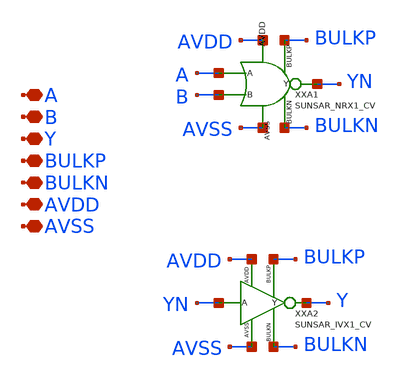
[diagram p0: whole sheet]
** sch_path: design/SUN_SAR9B_SKY130NM/SUNSAR_ORX1_CV.sch
**.subckt SUNSAR_ORX1_CV A B Y BULKP BULKN AVDD AVSS
*.iopin A
*.iopin B
*.iopin Y
*.iopin BULKP
*.iopin BULKN
*.iopin AVDD
*.iopin AVSS
XXA2 YN Y BULKP BULKN AVDD AVSS SUNSAR_IVX1_CV
**.ends
.end
